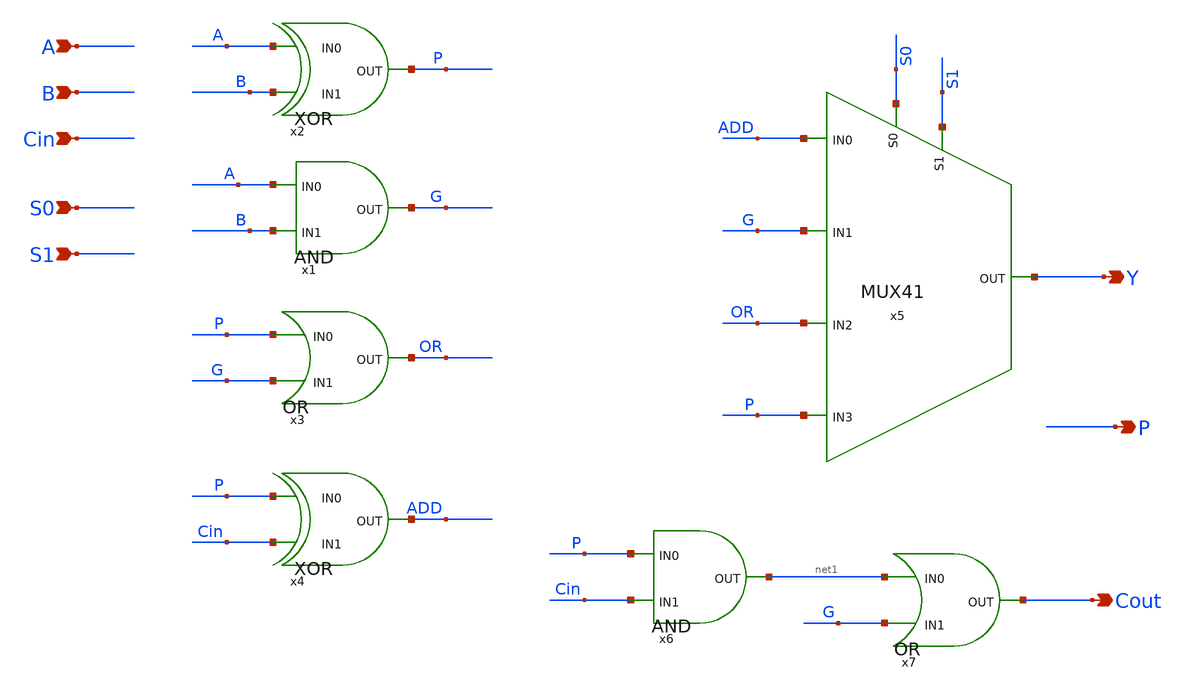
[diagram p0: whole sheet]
** sch_path: schematics/add/1bitblock.sch
**.subckt 1bitblock A B Cin S0 S1 Y Cout P
*.ipin A
*.ipin B
*.ipin Cin
*.ipin S0
*.ipin S1
*.opin Y
*.opin Cout
*.opin P
x1 A G B AND
x2 A B P XOR
x3 P G OR OR
x4 P Cin ADD XOR
x5 S0 ADD S1 G Y OR P MUX41
x6 P net1 Cin AND
x7 net1 G Cout OR
**.ends
.end
